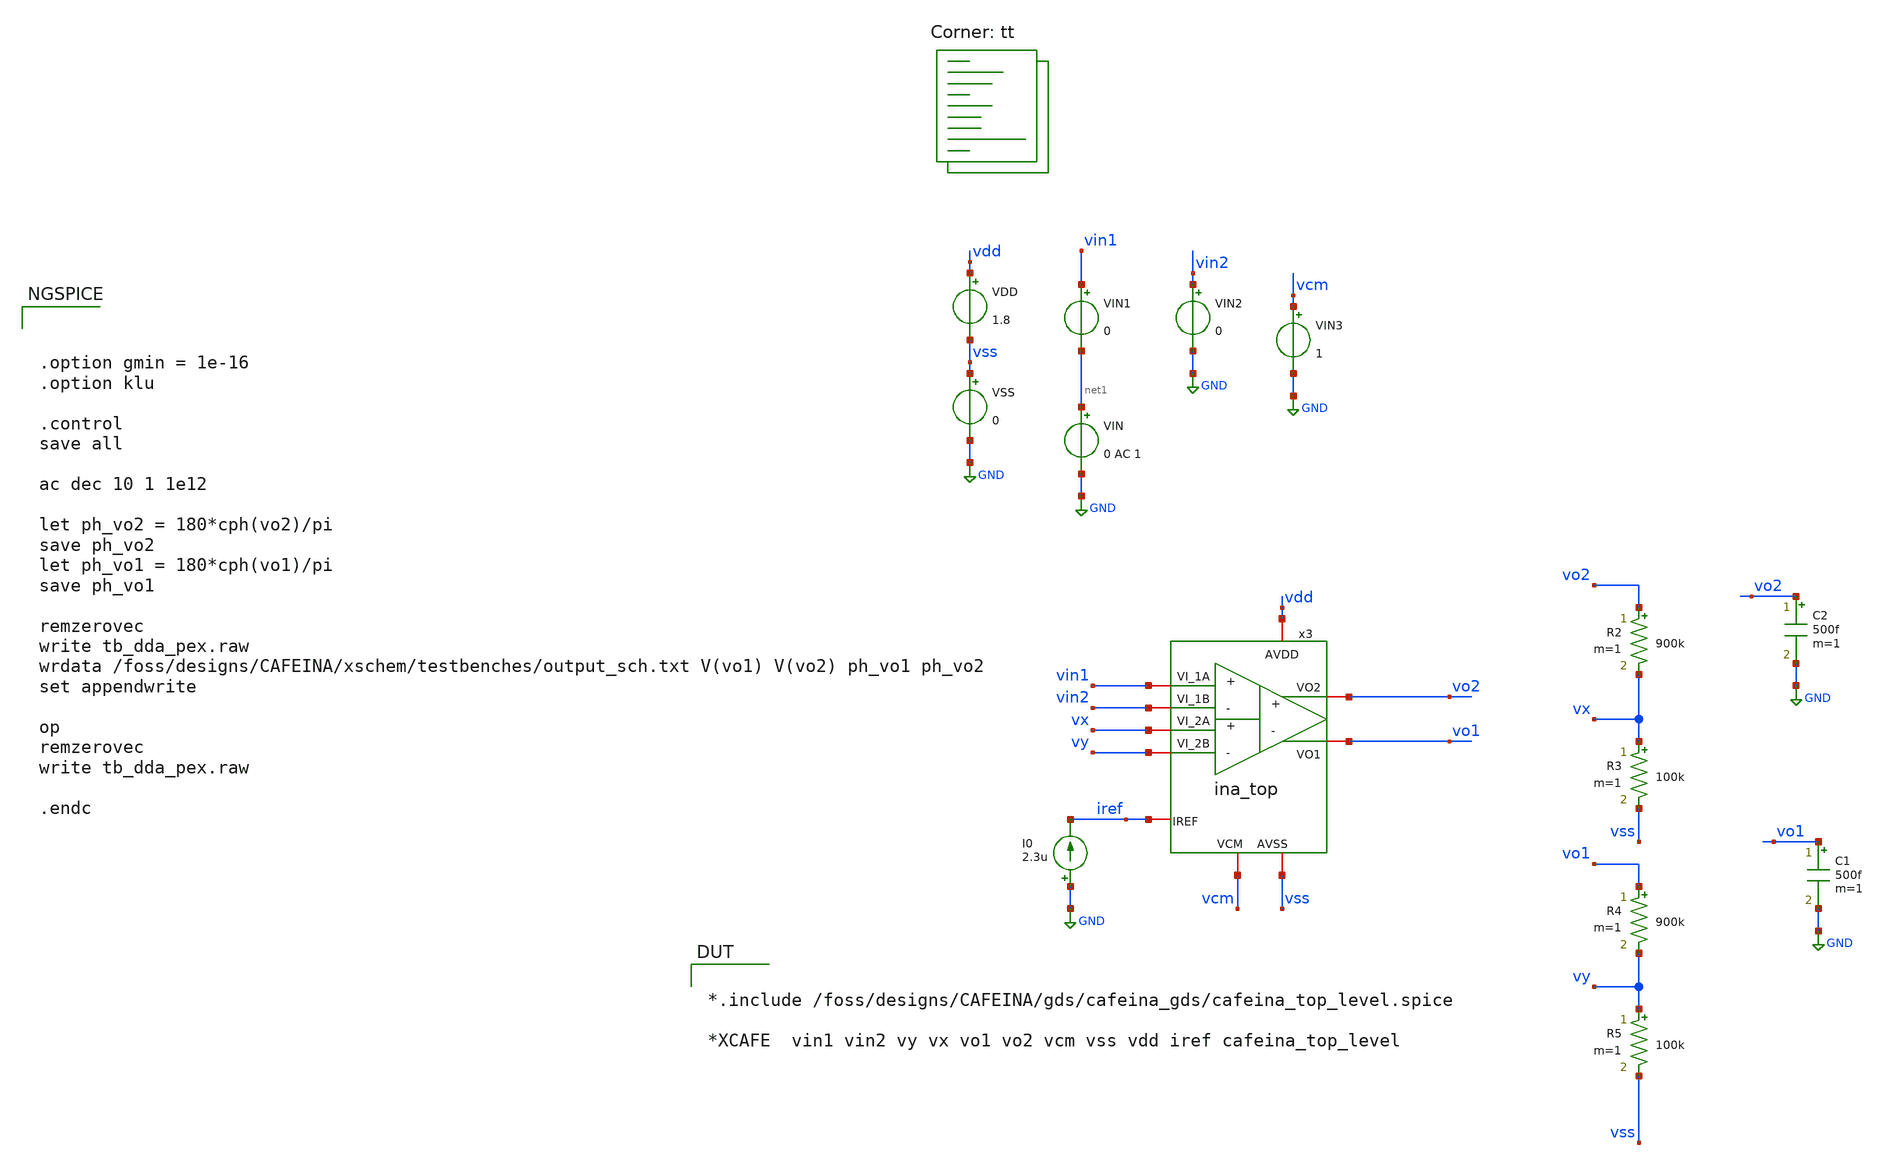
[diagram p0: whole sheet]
** sch_path: xschem/testbenches/tb_dda_pex.sch
**.subckt tb_dda_pex
VDD vdd vss 1.8
VSS vss GND 0
C1 vo1 GND 500f m=1
I0 GND iref 2.3u
VIN1 vin1 net1 0
VIN2 vin2 GND 0
VIN net1 GND 0 AC 1
C2 vo2 GND 500f m=1
VIN3 vcm GND 1
x3 vdd vss vin1 vin2 vo2 vo1 vcm iref vx vy ina_top
R2 vo2 vx 900k m=1
R3 vx vss 100k m=1
R4 vo1 vy 900k m=1
R5 vy vss 100k m=1
**** begin user architecture code



.option gmin = 1e-16
.option klu

.control
save all

ac dec 10 1 1e12

let ph_vo2 = 180*cph(vo2)/pi
save ph_vo2
let ph_vo1 = 180*cph(vo1)/pi
save ph_vo1

remzerovec
write tb_dda_pex.raw
wrdata /foss/designs/CAFEINA/xschem/testbenches/output_sch.txt V(vo1) V(vo2) ph_vo1 ph_vo2
set appendwrite

op
remzerovec
write tb_dda_pex.raw

.endc


.lib $::SKYWATER_MODELS/sky130.lib.spice tt


*.include /foss/designs/CAFEINA/gds/cafeina_gds/cafeina_top_level.spice

*XCAFE  vin1 vin2 vy vx vo1 vo2 vcm vss vdd iref cafeina_top_level



**** end user architecture code
**.ends
.GLOBAL GND
.end
